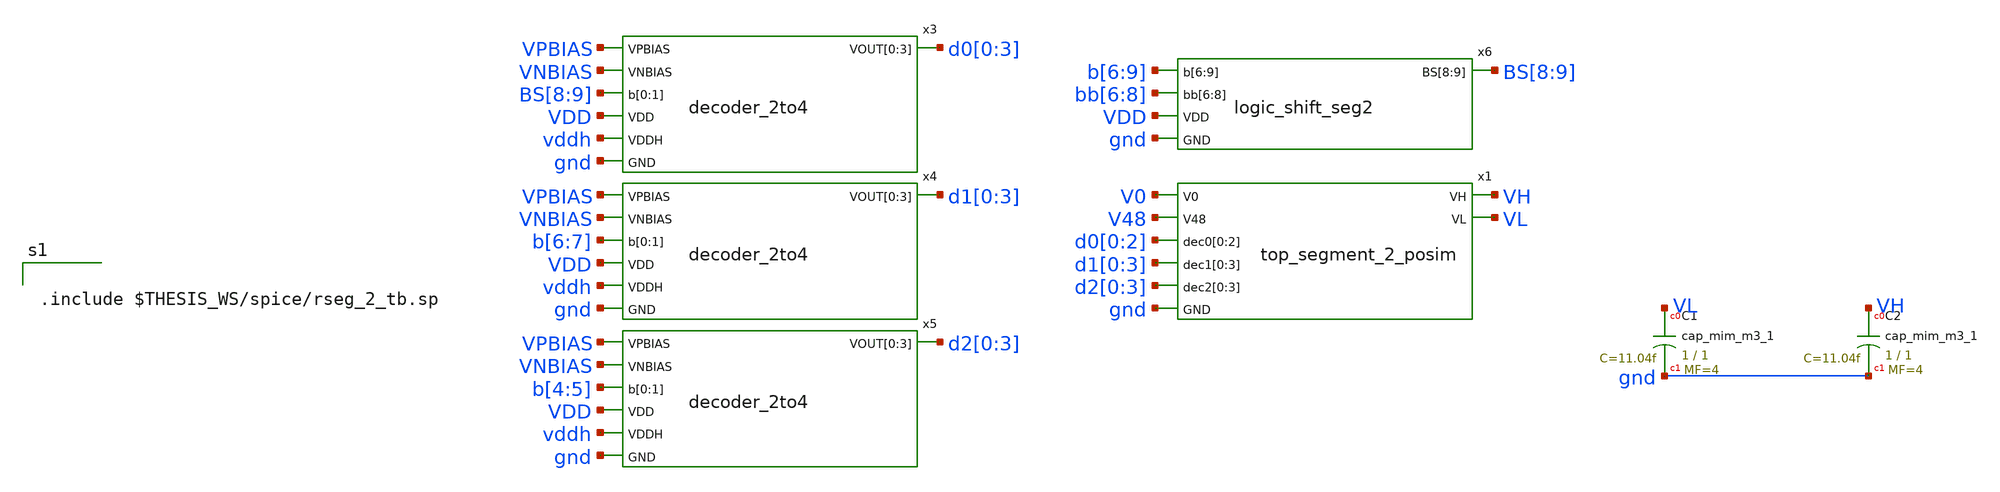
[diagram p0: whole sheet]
** sch_path: xschem/res_seg_2-tb.sch
.lib $::SKYWATER_MODELS/sky130.lib.spice tt
.include $::SKYWATER_STDCELLS/sky130_fd_sc_hd.spice

**.subckt res_seg_2-tb
XC1 VL gnd sky130_fd_pr__cap_mim_m3_1 W=1 L=1 MF=4 m=4
XC2 VH gnd sky130_fd_pr__cap_mim_m3_1 W=1 L=1 MF=4 m=4
x3 VPBIAS VNBIAS BS[8] BS[9] d0[0] d0[1] d0[2] d0[3] VDD vddh gnd decoder_2to4
x4 VPBIAS VNBIAS b[6] b[7] d1[0] d1[1] d1[2] d1[3] VDD vddh gnd decoder_2to4
x5 VPBIAS VNBIAS b[4] b[5] d2[0] d2[1] d2[2] d2[3] VDD vddh gnd decoder_2to4
x6 b[6] b[7] b[8] b[9] bb[6] bb[7] bb[8] BS[8] BS[9] VDD gnd logic_shift_seg2
x1 V0 V48 d0[0] d0[1] d0[2] d1[0] d1[1] d1[2] d1[3] d2[0] d2[1] d2[2] d2[3] VH VL gnd
+ top_segment_2_posim
**** begin user architecture code


.include $THESIS_WS/spice/rseg_2_tb.sp


**** end user architecture code
**.ends

* expanding   symbol:  decoder_2to4.sym # of pins=7
** sym_path: xschem/decoder_2to4.sym
** sch_path: xschem/decoder_2to4.sch
.subckt decoder_2to4 VPBIAS VNBIAS b[0] b[1] VOUT[0] VOUT[1] VOUT[2] VOUT[3] VDD VDDH GND
*.ipin VPBIAS
*.ipin VNBIAS
*.ipin b[0],b[1]
*.opin VOUT[0],VOUT[1],VOUT[2],VOUT[3]
*.ipin VDDH
*.ipin GND
*.ipin VDD
x1 VPBIAS VNBIAS DIN[0] VOUT[1] VOUT[2] VOUT[3] VOUT[0] VDDH GND VDDH GND pull_up_down_network
x2 VPBIAS VNBIAS DIN[1] VOUT[0] VOUT[2] VOUT[3] VOUT[1] VDDH GND VDDH GND pull_up_down_network
x3 VPBIAS VNBIAS DIN[2] VOUT[0] VOUT[1] VOUT[3] VOUT[2] VDDH GND VDDH GND pull_up_down_network
x4 VPBIAS VNBIAS DIN[3] VOUT[0] VOUT[1] VOUT[2] VOUT[3] VDDH GND VDDH GND pull_up_down_network
x6 bb[0] bb[1] DIN[0] VDD GND nand
x7 b[0] bb[1] DIN[1] VDD GND nand
x8 bb[0] b[1] DIN[2] VDD GND nand
x9 b[0] b[1] DIN[3] VDD GND nand
x5 b[0] bb[0] VDD GND inv
x10 b[1] bb[1] VDD GND inv
.ends


* expanding   symbol:  logic_shift_seg2.sym # of pins=5
** sym_path: xschem/logic_shift_seg2.sym
** sch_path: xschem/logic_shift_seg2.sch
.subckt logic_shift_seg2 b[6] b[7] b[8] b[9] bb[6] bb[7] bb[8] BS[8] BS[9] VDD GND
*.ipin b[6],b[7],b[8],b[9]
*.opin BS[8],BS[9]
*.ipin GND
*.ipin VDD
*.ipin bb[6],bb[7],bb[8]
x1 b[9] b[8] GND GND VDD VDD n1 sky130_fd_sc_hd__nand2_1
x2 b[9] b[7] GND GND VDD VDD n2 sky130_fd_sc_hd__nand2_1
x3 b[9] b[6] GND GND VDD VDD n3 sky130_fd_sc_hd__nand2_1
x5 bb[8] bb[7] bb[6] GND GND VDD VDD n6 sky130_fd_sc_hd__nand3_1
x4 n3 n2 n1 GND GND VDD VDD BS[9] sky130_fd_sc_hd__nand3_1
x6 b[6] b[8] GND GND VDD VDD n4 sky130_fd_sc_hd__nand2_1
x7 b[7] b[8] GND GND VDD VDD n5 sky130_fd_sc_hd__nand2_1
x8 n6 n5 n4 GND GND VDD VDD BS[8] sky130_fd_sc_hd__nand3_1
.ends


* expanding   symbol:  pull_up_down_network.sym # of pins=9
** sym_path: xschem/pull_up_down_network.sym
** sch_path: xschem/pull_up_down_network.sch
.subckt pull_up_down_network VPBIAS VNBIAS DIN V[0] V[1] V[2] VOUT VDDH GND VPB VNB
*.ipin VPBIAS
*.ipin VNBIAS
*.ipin DIN
*.ipin V[0],V[1],V[2]
*.opin VOUT
*.ipin VDDH
*.ipin GND
*.ipin VPB
*.ipin VNB
XM1 net2 VPBIAS VDDH VPB sky130_fd_pr__pfet_g5v0d10v5 L=l W=wp nf=1 ad='int((nf+1)/2) * W/nf * 0.29'
+ as='int((nf+2)/2) * W/nf * 0.29' pd='2*int((nf+1)/2) * (W/nf + 0.29)' ps='2*int((nf+2)/2) * (W/nf + 0.29)'
+ nrd='0.29 / W' nrs='0.29 / W' sa=0 sb=0 sd=0 mult=1 m=1
.param wp=0.84 wn=1 l=1

XM2 net3 V[0] net2 VPB sky130_fd_pr__pfet_g5v0d10v5 L=l W=wp nf=1 ad='int((nf+1)/2) * W/nf * 0.29' as='int((nf+2)/2) * W/nf * 0.29'
+ pd='2*int((nf+1)/2) * (W/nf + 0.29)' ps='2*int((nf+2)/2) * (W/nf + 0.29)' nrd='0.29 / W' nrs='0.29 / W'
+ sa=0 sb=0 sd=0 mult=1 m=1
XM3 net4 V[1] net3 VPB sky130_fd_pr__pfet_g5v0d10v5 L=l W=wp nf=1 ad='int((nf+1)/2) * W/nf * 0.29' as='int((nf+2)/2) * W/nf * 0.29'
+ pd='2*int((nf+1)/2) * (W/nf + 0.29)' ps='2*int((nf+2)/2) * (W/nf + 0.29)' nrd='0.29 / W' nrs='0.29 / W'
+ sa=0 sb=0 sd=0 mult=1 m=1
XM4 VOUT V[2] net4 VPB sky130_fd_pr__pfet_g5v0d10v5 L=l W=wp nf=1 ad='int((nf+1)/2) * W/nf * 0.29' as='int((nf+2)/2) * W/nf * 0.29'
+ pd='2*int((nf+1)/2) * (W/nf + 0.29)' ps='2*int((nf+2)/2) * (W/nf + 0.29)' nrd='0.29 / W' nrs='0.29 / W'
+ sa=0 sb=0 sd=0 mult=1 m=1
XM5 VOUT VNBIAS net1 VNB sky130_fd_pr__nfet_g5v0d10v5 L=l W=wn nf=1 ad='int((nf+1)/2) * W/nf * 0.29'
+ as='int((nf+2)/2) * W/nf * 0.29' pd='2*int((nf+1)/2) * (W/nf + 0.29)' ps='2*int((nf+2)/2) * (W/nf + 0.29)'
+ nrd='0.29 / W' nrs='0.29 / W' sa=0 sb=0 sd=0 mult=1 m=1
XM6 net1 DIN GND VNB sky130_fd_pr__nfet_01v8 L=0.15 W=2 nf=1 ad='int((nf+1)/2) * W/nf * 0.29' as='int((nf+2)/2) * W/nf * 0.29'
+ pd='2*int((nf+1)/2) * (W/nf + 0.29)' ps='2*int((nf+2)/2) * (W/nf + 0.29)' nrd='0.29 / W' nrs='0.29 / W'
+ sa=0 sb=0 sd=0 mult=1 m=1
.ends


* expanding   symbol:  nand.sym # of pins=5
** sym_path: xschem/nand.sym
** sch_path: xschem/nand.sch
.subckt nand in1 in2 out VDD GND
*.ipin in2
*.opin out
*.ipin VDD
*.ipin GND
*.ipin in1
.param wp=0.63 wn=0.42 l=0.15
XM1 out in1 VDD VDD sky130_fd_pr__pfet_01v8 L=l W=wp nf=1 ad='int((nf+1)/2) * W/nf * 0.29' as='int((nf+2)/2) * W/nf * 0.29'
+ pd='2*int((nf+1)/2) * (W/nf + 0.29)' ps='2*int((nf+2)/2) * (W/nf + 0.29)' nrd='0.29 / W' nrs='0.29 / W'
+ sa=0 sb=0 sd=0 mult=1 m=1
XM2 out in2 VDD VDD sky130_fd_pr__pfet_01v8 L=l W=wp nf=1 ad='int((nf+1)/2) * W/nf * 0.29' as='int((nf+2)/2) * W/nf * 0.29'
+ pd='2*int((nf+1)/2) * (W/nf + 0.29)' ps='2*int((nf+2)/2) * (W/nf + 0.29)' nrd='0.29 / W' nrs='0.29 / W'
+ sa=0 sb=0 sd=0 mult=1 m=1
XM3 out in2 net1 GND sky130_fd_pr__nfet_01v8 L=l W=wn nf=1 ad='int((nf+1)/2) * W/nf * 0.29' as='int((nf+2)/2) * W/nf * 0.29'
+ pd='2*int((nf+1)/2) * (W/nf + 0.29)' ps='2*int((nf+2)/2) * (W/nf + 0.29)' nrd='0.29 / W' nrs='0.29 / W'
+ sa=0 sb=0 sd=0 mult=1 m=1
XM4 net1 in1 GND GND sky130_fd_pr__nfet_01v8 L=l W=wn nf=1 ad='int((nf+1)/2) * W/nf * 0.29' as='int((nf+2)/2) * W/nf * 0.29'
+ pd='2*int((nf+1)/2) * (W/nf + 0.29)' ps='2*int((nf+2)/2) * (W/nf + 0.29)' nrd='0.29 / W' nrs='0.29 / W'
+ sa=0 sb=0 sd=0 mult=1 m=1
.ends


* expanding   symbol:  inv.sym # of pins=4
** sym_path: xschem/inv.sym
** sch_path: xschem/inv.sch
.subckt inv in out vdd gnd
*.ipin in
*.opin out
*.ipin vdd
*.ipin gnd
XM1 out in gnd gnd sky130_fd_pr__nfet_01v8 L=0.15 W=0.42 nf=1 ad='int((nf+1)/2) * W/nf * 0.29' as='int((nf+2)/2) * W/nf * 0.29'
+ pd='2*int((nf+1)/2) * (W/nf + 0.29)' ps='2*int((nf+2)/2) * (W/nf + 0.29)' nrd='0.29 / W' nrs='0.29 / W'
+ sa=0 sb=0 sd=0 mult=1 m=1
XM2 out in vdd vdd sky130_fd_pr__pfet_01v8 L=0.15 W=1.26 nf=1 ad='int((nf+1)/2) * W/nf * 0.29' as='int((nf+2)/2) * W/nf * 0.29'
+ pd='2*int((nf+1)/2) * (W/nf + 0.29)' ps='2*int((nf+2)/2) * (W/nf + 0.29)' nrd='0.29 / W' nrs='0.29 / W'
+ sa=0 sb=0 sd=0 mult=1 m=1
.ends

.end
